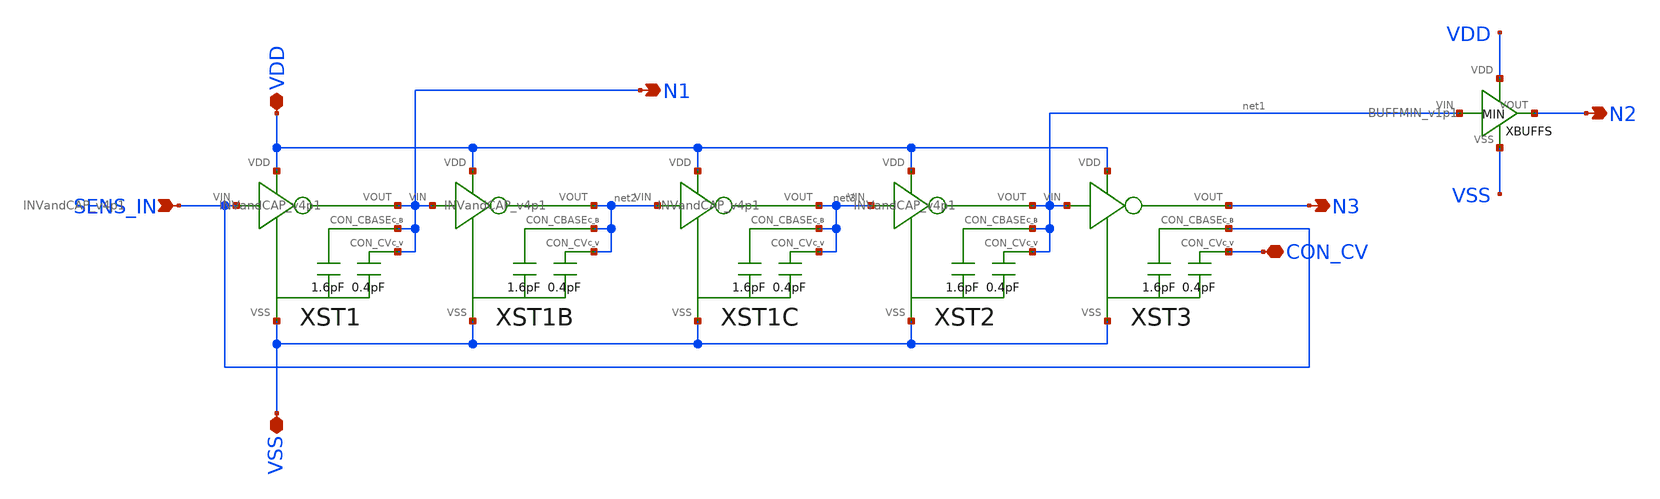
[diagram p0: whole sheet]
** sch_path: OSC_v7p1.sch
**.subckt OSC_v7p1 SENS_IN VDD VSS N1 N2 CON_CV N3
*.ipin SENS_IN
*.iopin VDD
*.iopin VSS
*.opin N1
*.opin N2
*.iopin CON_CV
*.opin N3
XST1 SENS_IN VDD VSS N1 N1 N1 INVandCAP_v4p1
XST2 net3 VDD VSS net1 net1 net1 INVandCAP_v4p1
XST3 net1 VDD VSS N3 CON_CV SENS_IN INVandCAP_v4p1
XBUFFS net1 N2 VDD VSS BUFFMIN_v1p1
XST1B N1 VDD VSS net2 net2 net2 INVandCAP_v4p1
XST1C net2 VDD VSS net3 net3 net3 INVandCAP_v4p1
**.ends
.end
